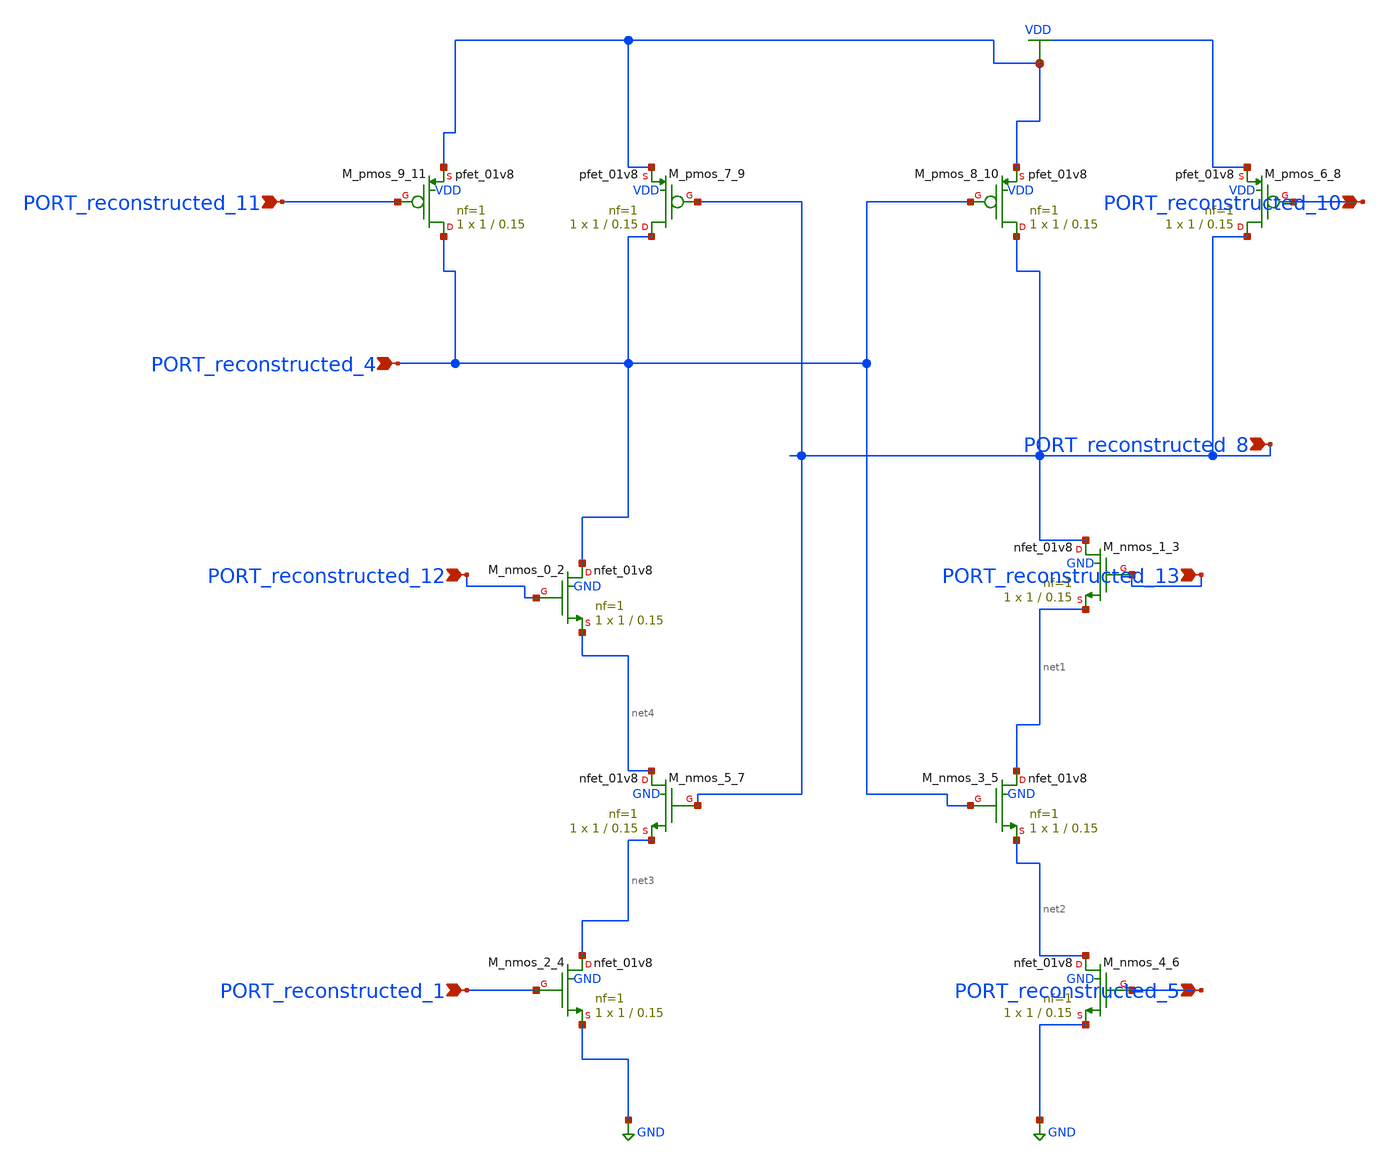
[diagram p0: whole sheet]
** sch_path: schematics/10_1007_s00034-017-0630-6_03_001_crop2.sch
**.subckt 10_1007_s00034-017-0630-6_03_001_crop2 PORT_reconstructed_12 PORT_reconstructed_4
*+ PORT_reconstructed_8 PORT_reconstructed_5 PORT_reconstructed_13 PORT_reconstructed_11 PORT_reconstructed_10
*+ PORT_reconstructed_1
*.ipin PORT_reconstructed_12
*.ipin PORT_reconstructed_4
*.ipin PORT_reconstructed_8
*.ipin PORT_reconstructed_5
*.ipin PORT_reconstructed_13
*.ipin PORT_reconstructed_11
*.ipin PORT_reconstructed_10
*.ipin PORT_reconstructed_1
XM_nmos_0_2 PORT_reconstructed_4 PORT_reconstructed_12 net4 GND sky130_fd_pr__nfet_01v8 L=0.15 W=1 nf=1
+ ad='int((1 + 1)/2) * 1 / 1 * 0.29' as='int((1 + 2)/2) * 1 / 1 * 0.29' pd='2*int((1 + 1)/2) * (1 / 1 + 0.29)'
+ ps='2*int((1 + 2)/2) * (1 / 1 + 0.29)' nrd='0.29 / 1 ' nrs='0.29 / 1 ' sa=0 sb=0 sd=0 mult=1 m=1
XM_nmos_1_3 PORT_reconstructed_8 PORT_reconstructed_13 net1 GND sky130_fd_pr__nfet_01v8 L=0.15 W=1 nf=1
+ ad='int((1 + 1)/2) * 1 / 1 * 0.29' as='int((1 + 2)/2) * 1 / 1 * 0.29' pd='2*int((1 + 1)/2) * (1 / 1 + 0.29)'
+ ps='2*int((1 + 2)/2) * (1 / 1 + 0.29)' nrd='0.29 / 1 ' nrs='0.29 / 1 ' sa=0 sb=0 sd=0 mult=1 m=1
XM_nmos_2_4 net3 PORT_reconstructed_1 GND GND sky130_fd_pr__nfet_01v8 L=0.15 W=1 nf=1 ad='int((1 + 1)/2) * 1 / 1 * 0.29'
+ as='int((1 + 2)/2) * 1 / 1 * 0.29' pd='2*int((1 + 1)/2) * (1 / 1 + 0.29)' ps='2*int((1 + 2)/2) * (1 / 1 + 0.29)'
+ nrd='0.29 / 1 ' nrs='0.29 / 1 ' sa=0 sb=0 sd=0 mult=1 m=1
XM_nmos_3_5 net1 PORT_reconstructed_4 net2 GND sky130_fd_pr__nfet_01v8 L=0.15 W=1 nf=1 ad='int((1 + 1)/2) * 1 / 1 * 0.29'
+ as='int((1 + 2)/2) * 1 / 1 * 0.29' pd='2*int((1 + 1)/2) * (1 / 1 + 0.29)' ps='2*int((1 + 2)/2) * (1 / 1 + 0.29)'
+ nrd='0.29 / 1 ' nrs='0.29 / 1 ' sa=0 sb=0 sd=0 mult=1 m=1
XM_nmos_4_6 net2 PORT_reconstructed_5 GND GND sky130_fd_pr__nfet_01v8 L=0.15 W=1 nf=1 ad='int((1 + 1)/2) * 1 / 1 * 0.29'
+ as='int((1 + 2)/2) * 1 / 1 * 0.29' pd='2*int((1 + 1)/2) * (1 / 1 + 0.29)' ps='2*int((1 + 2)/2) * (1 / 1 + 0.29)'
+ nrd='0.29 / 1 ' nrs='0.29 / 1 ' sa=0 sb=0 sd=0 mult=1 m=1
XM_nmos_5_7 net4 PORT_reconstructed_8 net3 GND sky130_fd_pr__nfet_01v8 L=0.15 W=1 nf=1 ad='int((1 + 1)/2) * 1 / 1 * 0.29'
+ as='int((1 + 2)/2) * 1 / 1 * 0.29' pd='2*int((1 + 1)/2) * (1 / 1 + 0.29)' ps='2*int((1 + 2)/2) * (1 / 1 + 0.29)'
+ nrd='0.29 / 1 ' nrs='0.29 / 1 ' sa=0 sb=0 sd=0 mult=1 m=1
XM_pmos_6_8 PORT_reconstructed_8 PORT_reconstructed_10 VDD VDD sky130_fd_pr__pfet_01v8 L=0.15 W=1 nf=1
+ ad='int((1 + 1)/2) * 1 / 1 * 0.29' as='int((1 + 2)/2) * 1 / 1 * 0.29' pd='2*int((1 + 1)/2) * (1 / 1 + 0.29)'
+ ps='2*int((1 + 2)/2) * (1 / 1 + 0.29)' nrd='0.29 / 1 ' nrs='0.29 / 1 ' sa=0 sb=0 sd=0 mult=1 m=1
XM_pmos_7_9 PORT_reconstructed_4 PORT_reconstructed_8 VDD VDD sky130_fd_pr__pfet_01v8 L=0.15 W=1 nf=1
+ ad='int((1 + 1)/2) * 1 / 1 * 0.29' as='int((1 + 2)/2) * 1 / 1 * 0.29' pd='2*int((1 + 1)/2) * (1 / 1 + 0.29)'
+ ps='2*int((1 + 2)/2) * (1 / 1 + 0.29)' nrd='0.29 / 1 ' nrs='0.29 / 1 ' sa=0 sb=0 sd=0 mult=1 m=1
XM_pmos_8_10 PORT_reconstructed_8 PORT_reconstructed_4 VDD VDD sky130_fd_pr__pfet_01v8 L=0.15 W=1 nf=1
+ ad='int((1 + 1)/2) * 1 / 1 * 0.29' as='int((1 + 2)/2) * 1 / 1 * 0.29' pd='2*int((1 + 1)/2) * (1 / 1 + 0.29)'
+ ps='2*int((1 + 2)/2) * (1 / 1 + 0.29)' nrd='0.29 / 1 ' nrs='0.29 / 1 ' sa=0 sb=0 sd=0 mult=1 m=1
XM_pmos_9_11 PORT_reconstructed_4 PORT_reconstructed_11 VDD VDD sky130_fd_pr__pfet_01v8 L=0.15 W=1 nf=1
+ ad='int((1 + 1)/2) * 1 / 1 * 0.29' as='int((1 + 2)/2) * 1 / 1 * 0.29' pd='2*int((1 + 1)/2) * (1 / 1 + 0.29)'
+ ps='2*int((1 + 2)/2) * (1 / 1 + 0.29)' nrd='0.29 / 1 ' nrs='0.29 / 1 ' sa=0 sb=0 sd=0 mult=1 m=1
**.ends
.GLOBAL GND
.GLOBAL VDD
.end
